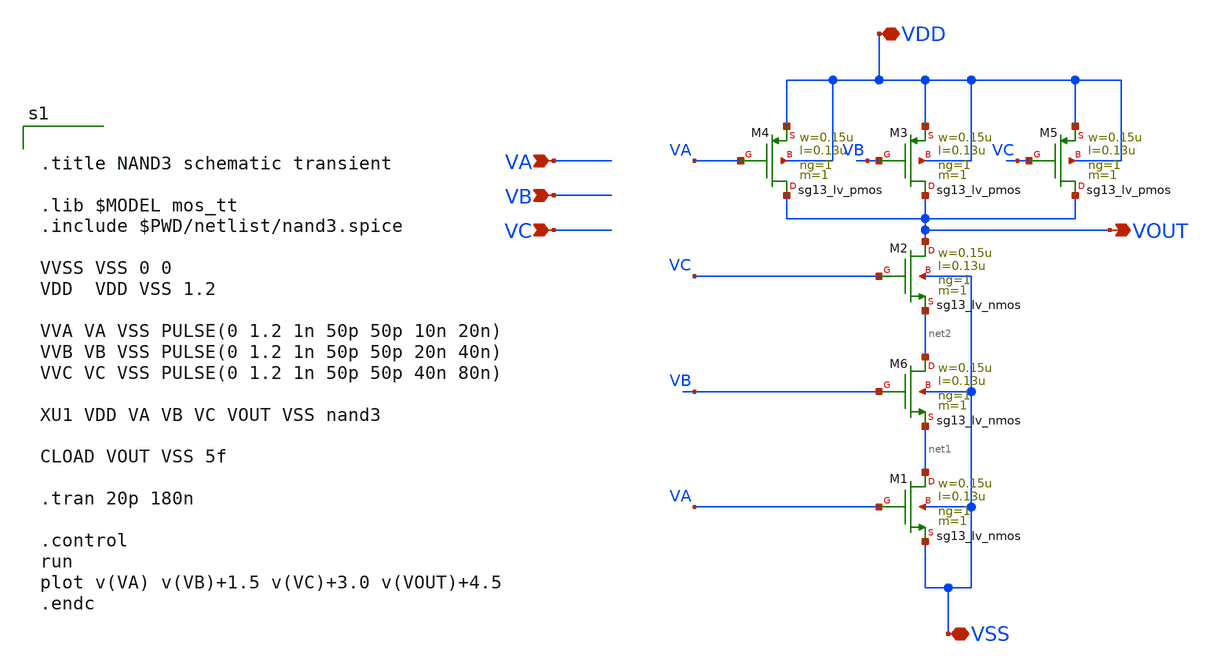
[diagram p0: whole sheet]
** sch_path: verification/testbenches/nand3/tb_nand3.sch
**.subckt tb_nand3 VDD VSS VA VB VOUT VC
*.iopin VDD
*.iopin VSS
*.ipin VA
*.ipin VB
*.opin VOUT
*.ipin VC
XM1 net1 VA VSS VSS sg13_lv_nmos w=0.15u l=0.13u ng=1 m=1 mm_ok=1
XM2 VOUT VC net2 VSS sg13_lv_nmos w=0.15u l=0.13u ng=1 m=1 mm_ok=1
XM3 VOUT VB VDD VDD sg13_lv_pmos w=0.15u l=0.13u ng=1 m=1 mm_ok=1
XM4 VOUT VA VDD VDD sg13_lv_pmos w=0.15u l=0.13u ng=1 m=1 mm_ok=1
XM5 VOUT VC VDD VDD sg13_lv_pmos w=0.15u l=0.13u ng=1 m=1 mm_ok=1
XM6 net2 VB net1 VSS sg13_lv_nmos w=0.15u l=0.13u ng=1 m=1 mm_ok=1
**** begin user architecture code


.title NAND3 schematic transient

.lib $MODEL mos_tt
.include $PWD/netlist/nand3.spice

VVSS VSS 0 0
VDD  VDD VSS 1.2

VVA VA VSS PULSE(0 1.2 1n 50p 50p 10n 20n)
VVB VB VSS PULSE(0 1.2 1n 50p 50p 20n 40n)
VVC VC VSS PULSE(0 1.2 1n 50p 50p 40n 80n)

XU1 VDD VA VB VC VOUT VSS nand3

CLOAD VOUT VSS 5f

.tran 20p 180n

.control
run
plot v(VA) v(VB)+1.5 v(VC)+3.0 v(VOUT)+4.5
.endc


**** end user architecture code
**.ends
.end
